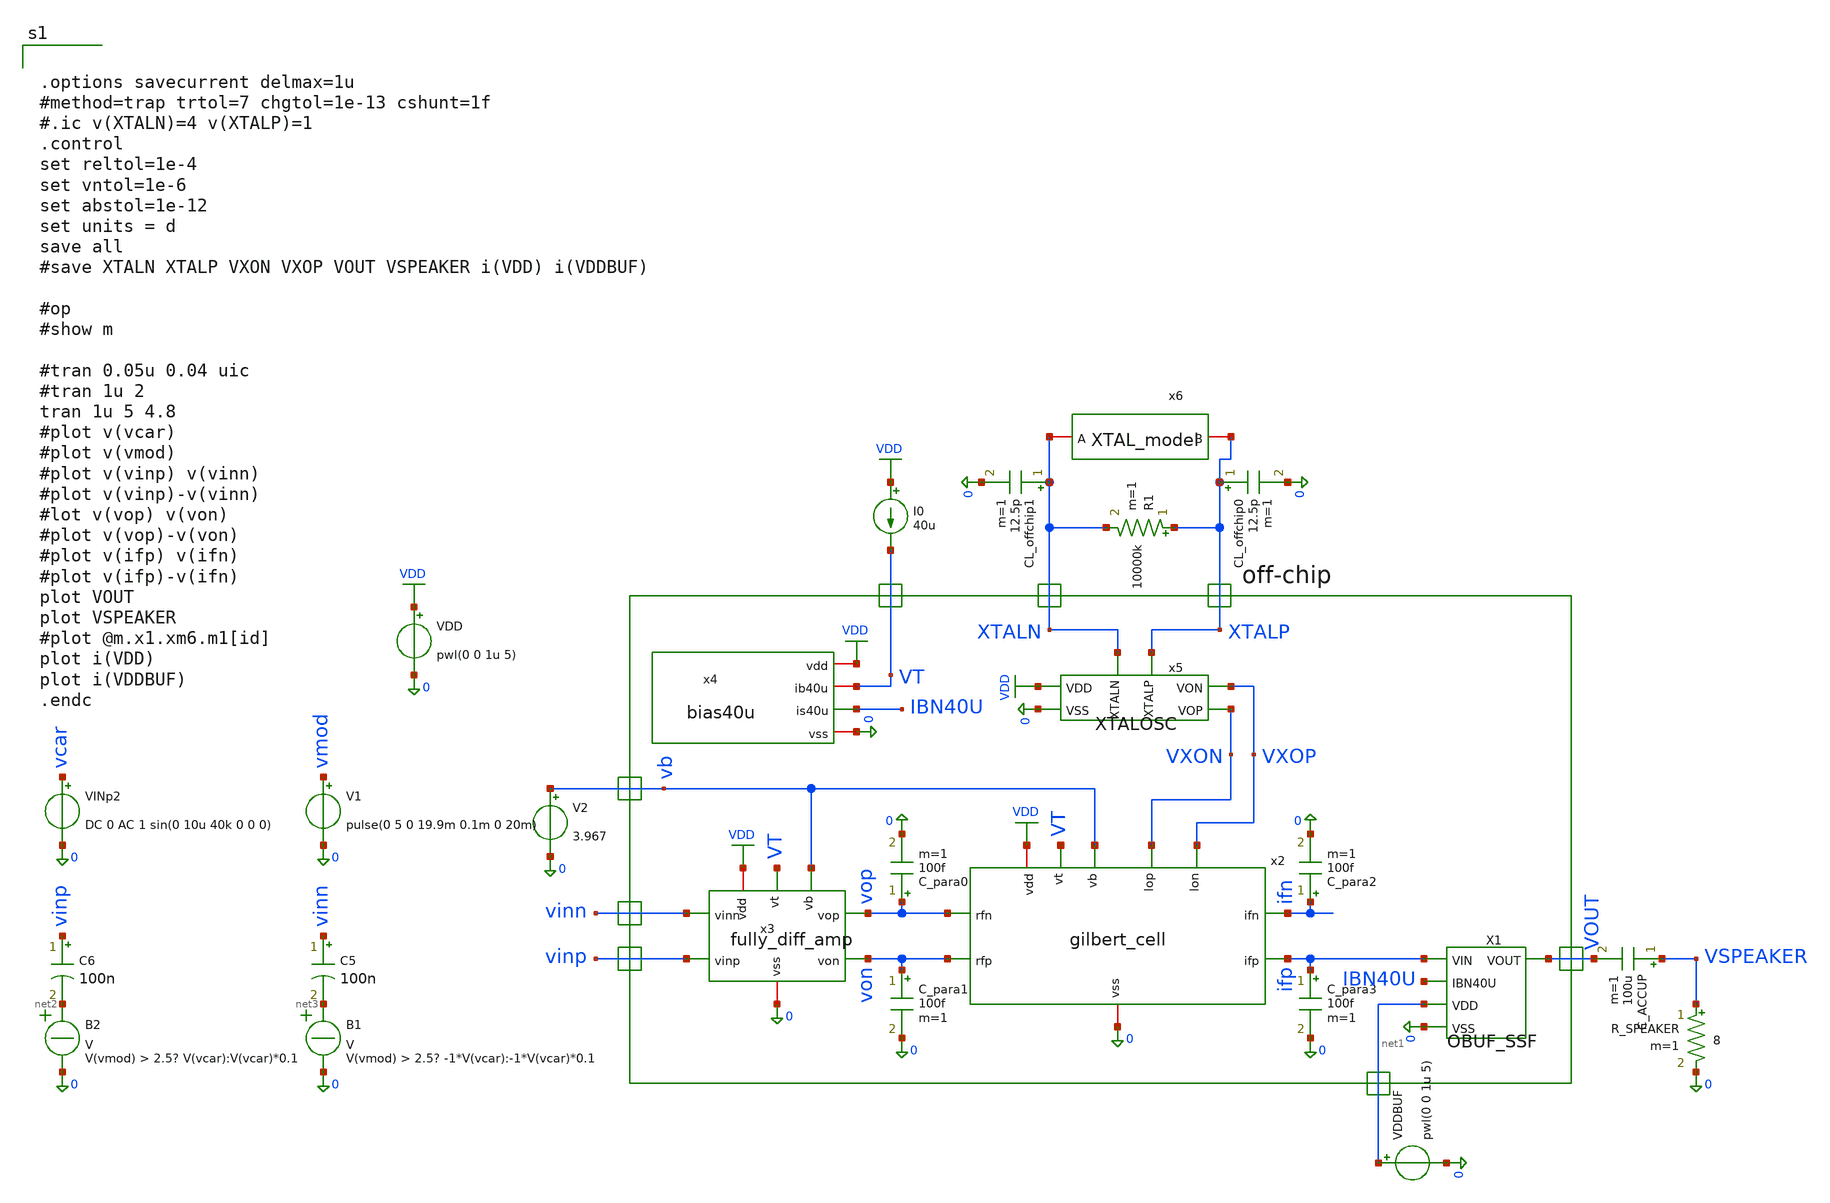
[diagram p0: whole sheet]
** sch_path: member_project/JJY_Receiver/Masahiro/jjy_recv/system_sim/cat_nyannyann.sch
**.subckt cat_nyannyann
I0 VDD VT 40u
C_para0 vop 0 100f m=1
C_para1 von 0 100f m=1
x2 vb ifn VDD ifp 0 VXON VXOP vop von VT gilbert_cell
C_para3 ifp 0 100f m=1
C_para2 ifn 0 100f m=1
x3 vb VDD vop von 0 vinn vinp VT fully_diff_amp
R_SPEAKER VSPEAKER 0 8 m=1
C_ACCUP VSPEAKER VOUT 100u m=1
CL_offchip0 XTALP 0 12.5p m=1
CL_offchip1 XTALN 0 12.5p m=1
x5 VDD 0 VXOP XTALN XTALP VXON XTALOSC
V2 vb 0 3.967
VINp2 vcar 0 DC 0 AC 1 sin(0 10u 40k 0 0 0)
V1 vmod 0 pulse(0 5 0 19.9m 0.1m 0 20m)
B2 net2 0 V = V(vmod) > 2.5? V(vcar):V(vcar)*0.1
B1 net3 0 V = V(vmod) > 2.5? -1*V(vcar):-1*V(vcar)*0.1
C5 vinn net3 100n m=1
C6 vinp net2 100n m=1
x4 VDD VT IBN40U 0 bias40u
VDDBUF net1 0 pwl(0 0 1u 5)
VDD VDD 0 pwl(0 0 1u 5)
x6 XTALN XTALP XTAL_model
R1 XTALP XTALN 10000k m=1
X1 net1 0 ifp VOUT IBN40U OBUF_SSF
**** begin user architecture code
 .include $::LIB/ip62_models


.options savecurrent delmax=1u
#method=trap trtol=7 chgtol=1e-13 cshunt=1f
#.ic v(XTALN)=4 v(XTALP)=1
.control
set reltol=1e-4
set vntol=1e-6
set abstol=1e-12
set units = d
save all
#save XTALN XTALP VXON VXOP VOUT VSPEAKER i(VDD) i(VDDBUF)

#op
#show m

#tran 0.05u 0.04 uic
#tran 1u 2
tran 1u 5 4.8
#plot v(vcar)
#plot v(vmod)
#plot v(vinp) v(vinn)
#plot v(vinp)-v(vinn)
#lot v(vop) v(von)
#plot v(vop)-v(von)
#plot v(ifp) v(ifn)
#plot v(ifp)-v(ifn)
plot VOUT
plot VSPEAKER
#plot @m.x1.xm6.m1[id]
plot i(VDD)
plot i(VDDBUF)
.endc


**** end user architecture code
**.ends
.GLOBAL VDD
.end
